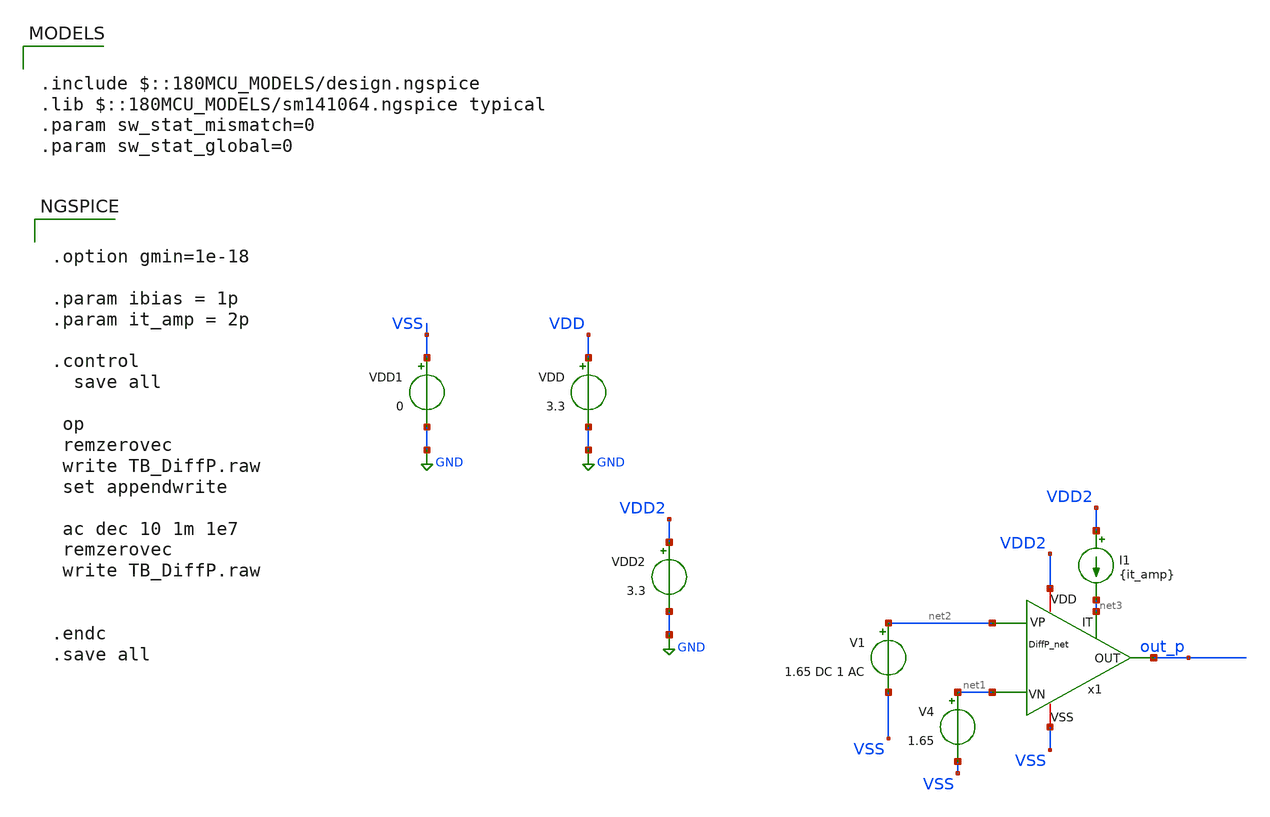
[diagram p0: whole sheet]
** sch_path: TIA_Filter/PseudoResistor/TB_DiffP.sch
**.subckt TB_DiffP
VDD VDD GND 3.3
V1 net2 VSS 1.65 DC 1 AC
V4 net1 VSS 1.65
I1 VDD2 net3 {it_amp}
x1 net1 net2 out_p net3 VDD2 VSS DiffP_net
VDD2 VDD2 GND 3.3
VDD1 VSS GND 0
**** begin user architecture code

.include $::180MCU_MODELS/design.ngspice
.lib $::180MCU_MODELS/sm141064.ngspice typical
.param sw_stat_mismatch=0
.param sw_stat_global=0



.option gmin=1e-18

.param ibias = 1p
.param it_amp = 2p

.control
  save all

 op
 remzerovec
 write TB_DiffP.raw
 set appendwrite

 ac dec 10 1m 1e7
 remzerovec
 write TB_DiffP.raw


.endc
.save all


**** end user architecture code
**.ends
.GLOBAL GND
.end
